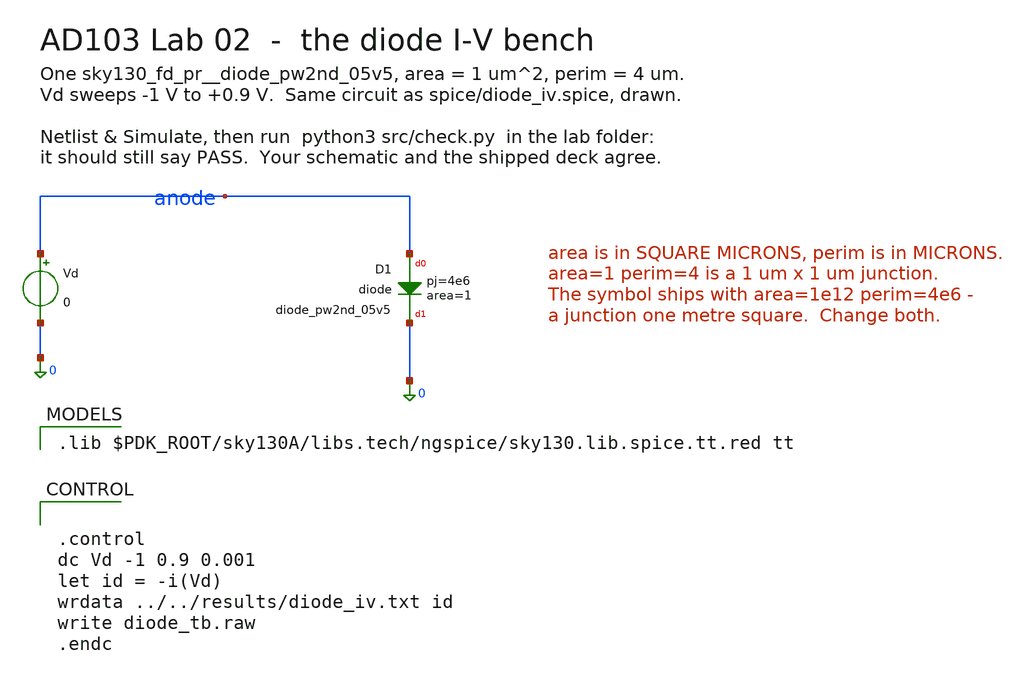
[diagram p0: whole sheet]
** sch_path: labs/lab-02-diode-iv/xschem/diode_tb.sch
**.subckt diode_tb
XD1 anode 0 sky130_fd_pr__diode_pw2nd_05v5 area=1 pj=4e6
Vd anode 0 0
**** begin user architecture code

.lib $PDK_ROOT/sky130A/libs.tech/ngspice/sky130.lib.spice.tt.red tt



.control
dc Vd -1 0.9 0.001
let id = -i(Vd)
wrdata ../../results/diode_iv.txt id
write diode_tb.raw
.endc


**** end user architecture code
**.ends
.end
